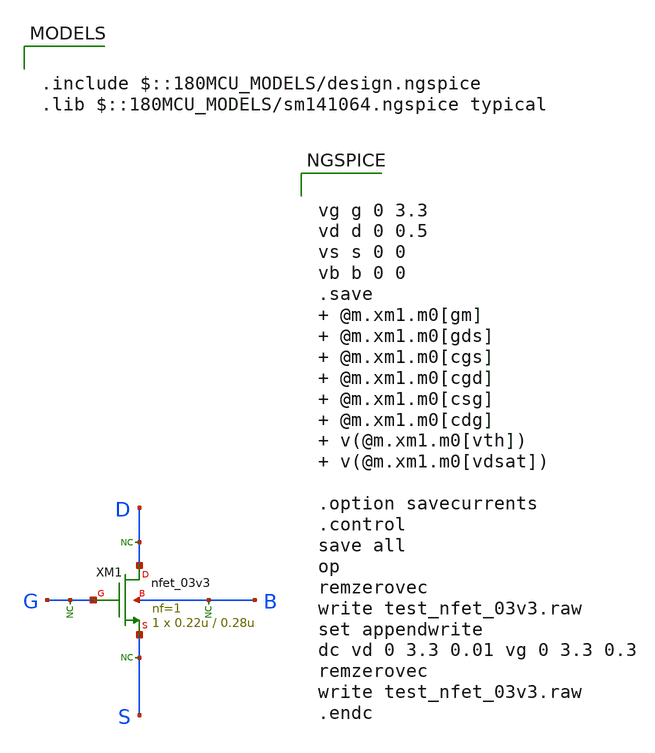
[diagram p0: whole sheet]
** sch_path: cells/xschem/tests/test_nfet_03v3.sch
* Copyright 2022 GlobalFoundries PDK Authors
* Licensed under the Apache License, Version 2.0 (the "License");
* you may not use this file except in compliance with the License.
* You may obtain a copy of the License at
* https://www.apache.org/licenses/LICENSE-2.0
* Unless required by applicable law or agreed to in writing, software
* distributed under the License is distributed on an "AS IS" BASIS,
* WITHOUT WARRANTIES OR CONDITIONS OF ANY KIND, either express or implied.
* See the License for the specific language governing permissions and
* limitations under the License.
**.subckt test_nfet_03v3
XM1 D G S B nfet_03v3 L=0.28u W=0.22u nf=1 ad='int((nf+1)/2) * W/nf * 0.18u' as='int((nf+2)/2) * W/nf * 0.18u'
+ pd='2*int((nf+1)/2) * (W/nf + 0.18u)' ps='2*int((nf+2)/2) * (W/nf + 0.18u)' nrd='0.18u / W' nrs='0.18u / W'
+ sa=0 sb=0 sd=0 m=1
* noconn D
* noconn S
* noconn G
* noconn B
**** begin user architecture code

.include $::180MCU_MODELS/design.ngspice
.lib $::180MCU_MODELS/sm141064.ngspice typical



vg g 0 3.3
vd d 0 0.5
vs s 0 0
vb b 0 0
.save  @m.xm1.m0[gm]  @m.xm1.m0[gds]  @m.xm1.m0[cgs]  @m.xm1.m0[cgd]  @m.xm1.m0[csg]  @m.xm1.m0[cdg]  v(@m.xm1.m0[vth])  v(@m.xm1.m0[vdsat])

.option savecurrents
.control
save all
op
remzerovec
write test_nfet_03v3.raw
set appendwrite
dc vd 0 3.3 0.01 vg 0 3.3 0.3
remzerovec
write test_nfet_03v3.raw
.endc


**** end user architecture code
**.ends
.end
